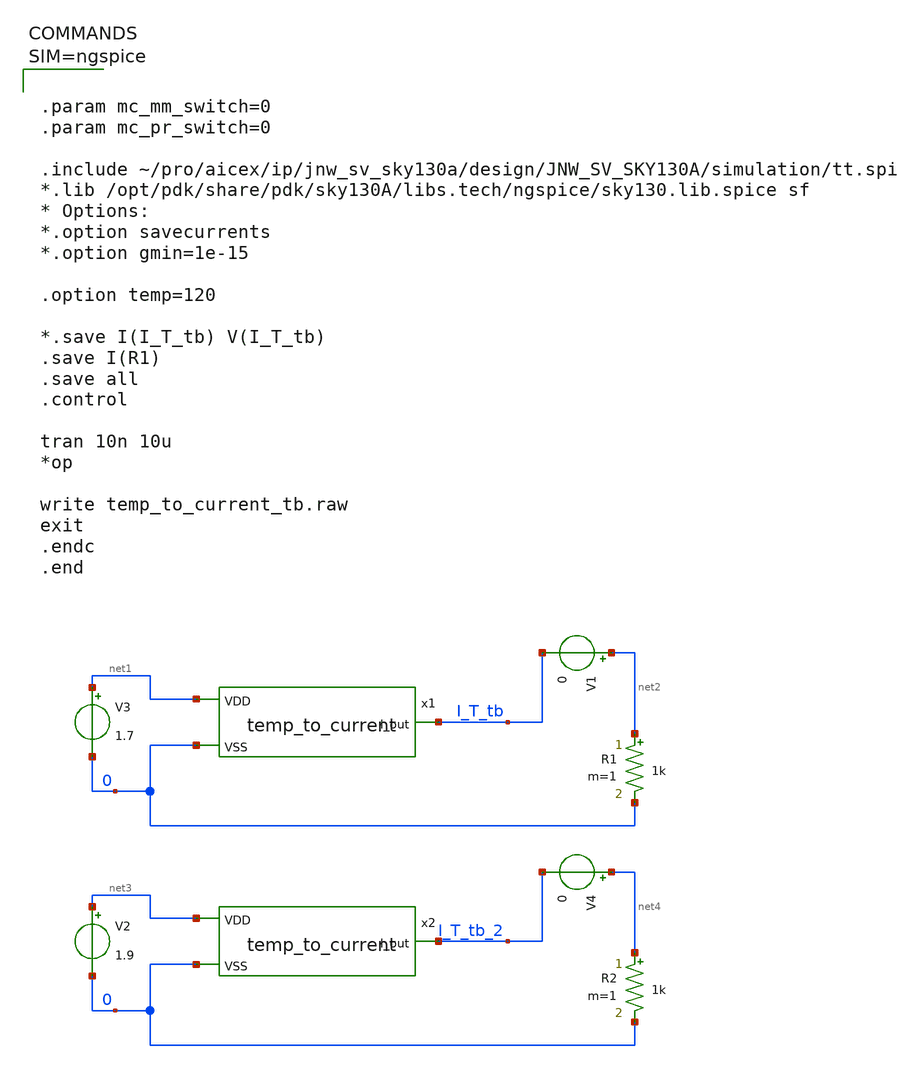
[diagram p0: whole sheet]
** sch_path: design/JNW_GR07_SKY130A/temp_to_current_tb.sch
**.subckt temp_to_current_tb
x1 net1 I_T_tb 0 temp_to_current
V3 net1 0 1.7
R1 net2 0 1k m=1
V1 net2 I_T_tb 0
x2 net3 I_T_tb_2 0 temp_to_current
V2 net3 0 1.9
R2 net4 0 1k m=1
V4 net4 I_T_tb_2 0
**** begin user architecture code



.param mc_mm_switch=0
.param mc_pr_switch=0

.include ~/pro/aicex/ip/jnw_sv_sky130a/design/JNW_SV_SKY130A/simulation/tt.spi
*.lib /opt/pdk/share/pdk/sky130A/libs.tech/ngspice/sky130.lib.spice sf
* Options:
*.option savecurrents
*.option gmin=1e-15

.option temp=120

*.save I(I_T_tb) V(I_T_tb)
.save I(R1)
.save all
.control

tran 10n 10u
*op

write temp_to_current_tb.raw
exit
.endc
.end



**** end user architecture code
**.ends
.end
